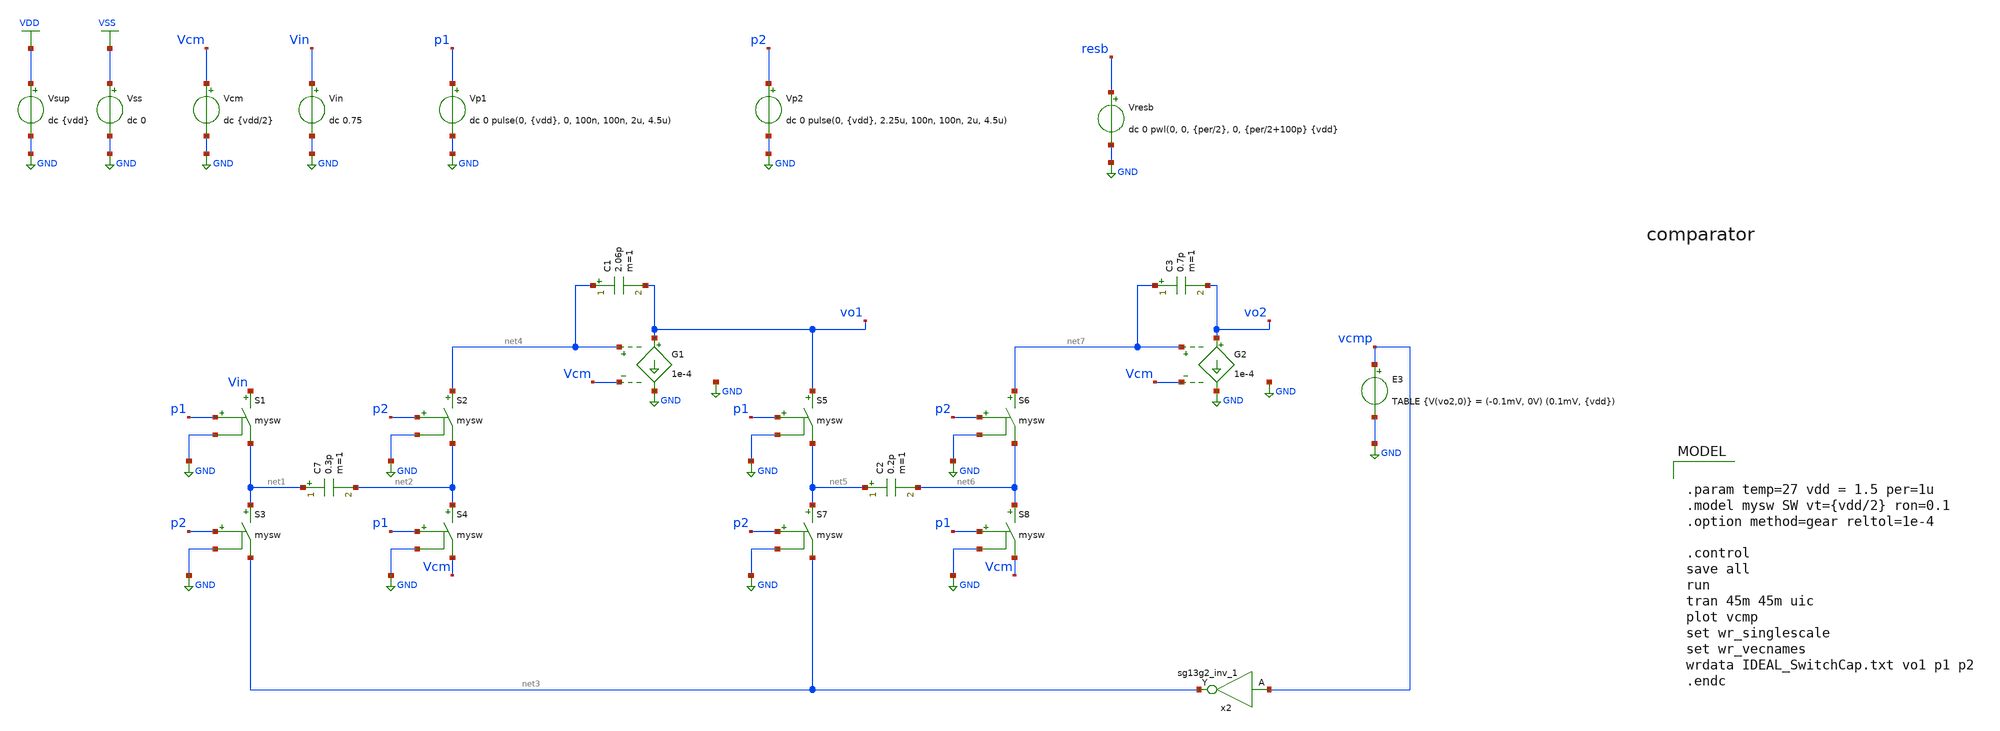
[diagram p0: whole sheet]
** sch_path: DSM/Schematics/IC_Designs_Hrishi/IdealCircuits/IDEAL_DSM.sch
**.subckt IDEAL_DSM
Vcm Vcm GND dc {vdd/2}
Vin Vin GND dc 0.75
Vp1 p1 GND dc 0 pulse(0, {vdd}, 0, 100n, 100n, 2u, 4.5u)
Vp2 p2 GND dc 0 pulse(0, {vdd}, 2.25u, 100n, 100n, 2u, 4.5u)
S1 Vin net1 p1 GND mysw
S2 net4 net2 p2 GND mysw
S3 net1 net3 p2 GND mysw
S4 net2 Vcm p1 GND mysw
C7 net1 net2 0.3p m=1
C1 net4 vo1 2.06p m=1
S5 vo1 net5 p1 GND mysw
S6 net7 net6 p2 GND mysw
S7 net5 net3 p2 GND mysw
S8 net6 Vcm p1 GND mysw
C2 net5 net6 0.2p m=1
C3 net7 vo2 0.7p m=1
E3 vcmp GND TABLE {V(vo2,0)} = (-0.1mV, 0V) (0.1mV, {vdd})
x2 net3 vcmp 1.5 0 sg13g2_inv_1
Vresb resb GND dc 0 pwl(0, 0, {per/2}, 0, {per/2+100p} {vdd}
Vsup VDD GND dc {vdd}
Vss VSS GND dc 0
G1 vo1 GND net4 Vcm 1e-4
G2 vo2 GND net7 Vcm 1e-4
**** begin user architecture code

.lib $::SG13G2_MODELS/cornerMOSlv.lib mos_tt
.lib $::SG13G2_MODELS/cornerRES.lib res_typ
.inc /foss/pdks/sg13g2/libs.ref/sg13g2_stdcell/spice/sg13g2_stdcell.spice


.param temp=27 vdd = 1.5 per=1u
.model mysw SW vt={vdd/2} ron=0.1
.option method=gear reltol=1e-4

.control
save all
run
tran 45m 45m uic
plot vcmp
set wr_singlescale
set wr_vecnames
wrdata IDEAL_SwitchCap.txt vo1 p1 p2
.endc

**** end user architecture code
**.ends

* expanding   symbol:  sg13g2_stdcells/sg13g2_inv_1.sym # of pins=2
** sym_path: sg13g2_stdcells/sg13g2_inv_1.sym
** sch_path: sg13g2_stdcells/sg13g2_inv_1.sch
.subckt sg13g2_inv_1 Y A VDD VSS
*.opin Y
*.ipin A
*.iopin VDD
*.iopin VSS
XM1 Y A VSS VSS sg13_lv_nmos w=740.00n l=130.00n ng=1 m=1 mm_ok=1
XM2 Y A VDD VDD sg13_lv_pmos w=1.12u l=130.00n ng=1 m=1 mm_ok=1
.ends

.GLOBAL GND
.GLOBAL VDD
.GLOBAL VSS
.end
